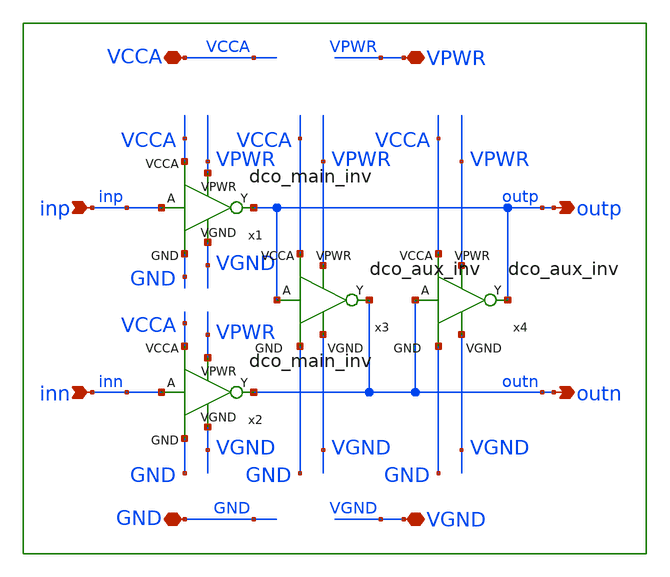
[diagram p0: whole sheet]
** sch_path: xschem/lib_dco/dco_cc_inv.sch
**.subckt dco_cc_inv outp inn VGND outn inp VPWR VCCA GND
*.opin outp
*.ipin inn
*.iopin VGND
*.opin outn
*.ipin inp
*.iopin VPWR
*.iopin VCCA
*.iopin GND
x1 VPWR VCCA outp GND VGND inp dco_main_inv
x2 VPWR VCCA outn GND VGND inn dco_main_inv
x3 VPWR VCCA outp outn GND VGND dco_aux_inv
x4 VPWR VCCA outn outp GND VGND dco_aux_inv
**.ends

* expanding   symbol:  /home/toind/work/vco_adc2/xschem/lib_dco/dco_main_inv.sym # of pins=6
** sym_path: xschem/lib_dco/dco_main_inv.sym
** sch_path: xschem/lib_dco/dco_main_inv.sch
.subckt dco_main_inv VPWR VCCA Y GND VGND A
*.iopin VPWR
*.iopin VGND
*.ipin A
*.opin Y
*.iopin VCCA
*.iopin GND
XM3 Y A VGND GND sky130_fd_pr__nfet_01v8 L=1 W=4 nf=2 ad='int((nf+1)/2) * W/nf * 0.29' as='int((nf+2)/2) * W/nf * 0.29'
+ pd='2*int((nf+1)/2) * (W/nf + 0.29)' ps='2*int((nf+2)/2) * (W/nf + 0.29)' nrd='0.29 / W' nrs='0.29 / W'
+ sa=0 sb=0 sd=0 mult=1 m=1
XM4 Y A VPWR VCCA sky130_fd_pr__pfet_01v8 L=1 W=6 nf=2 ad='int((nf+1)/2) * W/nf * 0.29' as='int((nf+2)/2) * W/nf * 0.29'
+ pd='2*int((nf+1)/2) * (W/nf + 0.29)' ps='2*int((nf+2)/2) * (W/nf + 0.29)' nrd='0.29 / W' nrs='0.29 / W'
+ sa=0 sb=0 sd=0 mult=1 m=1
.ends


* expanding   symbol:  /home/toind/work/vco_adc2/xschem/lib_dco/dco_aux_inv.sym # of pins=6
** sym_path: xschem/lib_dco/dco_aux_inv.sym
** sch_path: xschem/lib_dco/dco_aux_inv.sch
.subckt dco_aux_inv VPWR VCCA A Y GND VGND
*.iopin VPWR
*.iopin VGND
*.ipin A
*.opin Y
*.iopin VCCA
*.iopin GND
XM3 Y A VGND GND sky130_fd_pr__nfet_01v8 L=1 W=2 nf=1 ad='int((nf+1)/2) * W/nf * 0.29' as='int((nf+2)/2) * W/nf * 0.29'
+ pd='2*int((nf+1)/2) * (W/nf + 0.29)' ps='2*int((nf+2)/2) * (W/nf + 0.29)' nrd='0.29 / W' nrs='0.29 / W'
+ sa=0 sb=0 sd=0 mult=1 m=1
XM4 Y A VPWR VCCA sky130_fd_pr__pfet_01v8 L=1 W=3 nf=1 ad='int((nf+1)/2) * W/nf * 0.29' as='int((nf+2)/2) * W/nf * 0.29'
+ pd='2*int((nf+1)/2) * (W/nf + 0.29)' ps='2*int((nf+2)/2) * (W/nf + 0.29)' nrd='0.29 / W' nrs='0.29 / W'
+ sa=0 sb=0 sd=0 mult=1 m=1
.ends

.end
